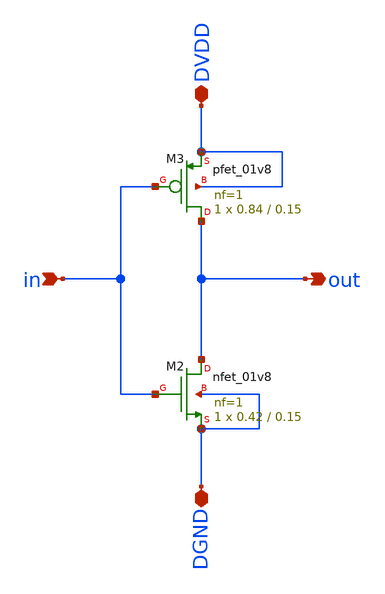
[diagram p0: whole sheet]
** sch_path: assignments/assignment4/inv.sch
**.subckt inv in out DVDD DGND
*.ipin in
*.opin out
*.iopin DVDD
*.iopin DGND
XM3 out in DVDD DVDD sky130_fd_pr__pfet_01v8 L=0.15 W=0.84 nf=1 ad='int((nf+1)/2) * W/nf * 0.29' as='int((nf+2)/2) * W/nf * 0.29'
+ pd='2*int((nf+1)/2) * (W/nf + 0.29)' ps='2*int((nf+2)/2) * (W/nf + 0.29)' nrd='0.29 / W' nrs='0.29 / W'
+ sa=0 sb=0 sd=0 mult=1 m=1
XM2 out in DGND DGND sky130_fd_pr__nfet_01v8 L=0.15 W=0.42 nf=1 ad='int((nf+1)/2) * W/nf * 0.29' as='int((nf+2)/2) * W/nf * 0.29'
+ pd='2*int((nf+1)/2) * (W/nf + 0.29)' ps='2*int((nf+2)/2) * (W/nf + 0.29)' nrd='0.29 / W' nrs='0.29 / W'
+ sa=0 sb=0 sd=0 mult=1 m=1
**.ends
.end
